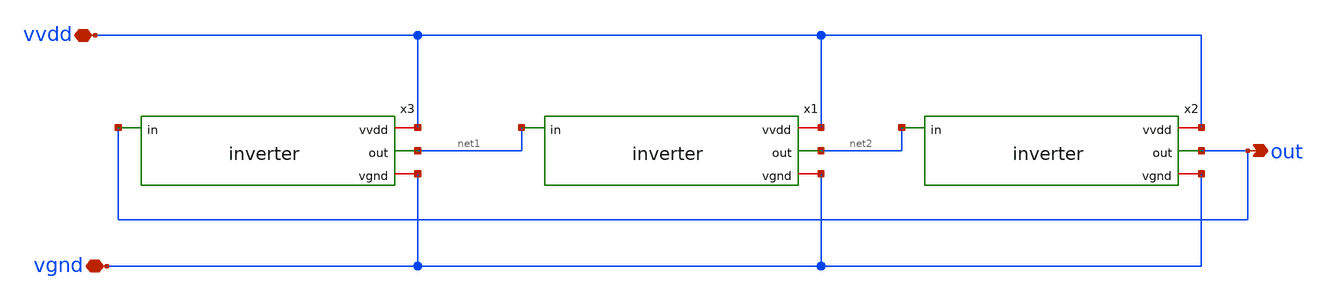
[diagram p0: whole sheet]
** sch_path: ringosc.sch
**.subckt ringosc vvdd vgnd out
*.iopin vvdd
*.iopin vgnd
*.opin out
x1 vvdd net2 net1 vgnd inverter
x2 vvdd out net2 vgnd inverter
x3 vvdd net1 out vgnd inverter
**.ends

* expanding   symbol:  inverter.sym # of pins=4
** sym_path: inverter.sym
** sch_path: inverter.sch
.subckt inverter vvdd out in vgnd
*.ipin in
*.opin out
*.iopin vvdd
*.iopin vgnd
XM1 out in vgnd vgnd sky130_fd_pr__nfet_01v8 L=0.15 W=1 nf=1 ad='int((nf+1)/2) * W/nf * 0.29' as='int((nf+2)/2) * W/nf * 0.29'
+ pd='2*int((nf+1)/2) * (W/nf + 0.29)' ps='2*int((nf+2)/2) * (W/nf + 0.29)' nrd='0.29 / W' nrs='0.29 / W'
+ sa=0 sb=0 sd=0 mult=1 m=1
XM2 out in vvdd vvdd sky130_fd_pr__pfet_01v8 L=0.15 W=1 nf=1 ad='int((nf+1)/2) * W/nf * 0.29' as='int((nf+2)/2) * W/nf * 0.29'
+ pd='2*int((nf+1)/2) * (W/nf + 0.29)' ps='2*int((nf+2)/2) * (W/nf + 0.29)' nrd='0.29 / W' nrs='0.29 / W'
+ sa=0 sb=0 sd=0 mult=1 m=1
.ends

.end
